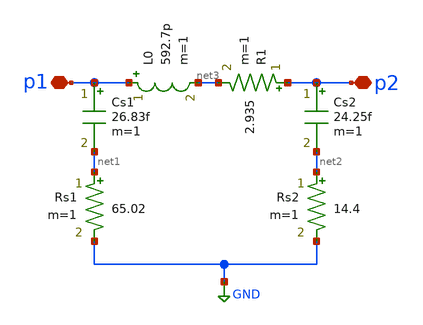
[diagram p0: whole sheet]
** sch_path: impedance-transformer/xschem/l1.sch
**.subckt l1 p2 p1
*.iopin p2
*.iopin p1
L0 p1 net3 592.7p m=1
Cs1 p1 net1 26.83f m=1
Cs2 p2 net2 24.25f m=1
Rs1 net1 GND 65.02 m=1
Rs2 net2 GND 14.4 m=1
R1 p2 net3 2.935 m=1
**.ends
.GLOBAL GND
.end
